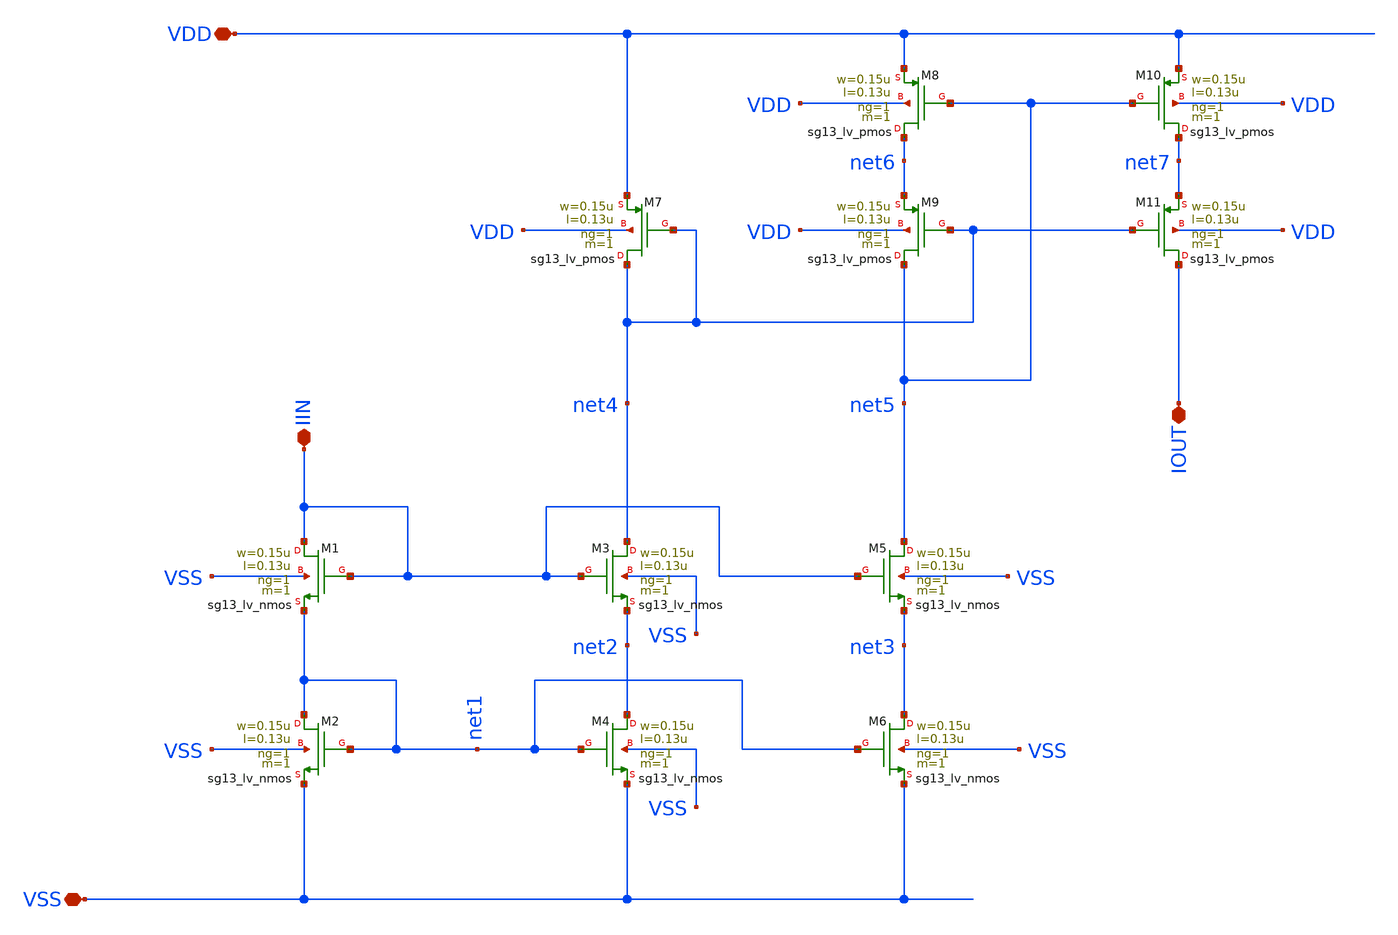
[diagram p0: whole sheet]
** sch_path: analog-db/templates/current_mirror/pmos_current_source/wide_swing_current_mirror_pmos.sch
* Copyright 2026 MacAnalog Research Group
**.subckt wide_swing_current_mirror_pmos VSS IIN VDD IOUT
*.iopin VSS
*.iopin IIN
*.iopin VDD
*.iopin IOUT
XM1 IIN IIN net1 VSS sg13_lv_nmos w=0.15u l=0.13u ng=1 m=1 mm_ok=1
XM2 net1 net1 VSS VSS sg13_lv_nmos w=0.15u l=0.13u ng=1 m=1 mm_ok=1
XM3 net4 IIN net2 VSS sg13_lv_nmos w=0.15u l=0.13u ng=1 m=1 mm_ok=1
XM4 net2 net1 VSS VSS sg13_lv_nmos w=0.15u l=0.13u ng=1 m=1 mm_ok=1
XM5 net5 IIN net3 VSS sg13_lv_nmos w=0.15u l=0.13u ng=1 m=1 mm_ok=1
XM6 net3 net1 VSS VSS sg13_lv_nmos w=0.15u l=0.13u ng=1 m=1 mm_ok=1
XM7 net4 net4 VDD VDD sg13_lv_pmos w=0.15u l=0.13u ng=1 m=1 mm_ok=1
XM8 net6 net5 VDD VDD sg13_lv_pmos w=0.15u l=0.13u ng=1 m=1 mm_ok=1
XM9 net5 net4 net6 VDD sg13_lv_pmos w=0.15u l=0.13u ng=1 m=1 mm_ok=1
XM10 net7 net5 VDD VDD sg13_lv_pmos w=0.15u l=0.13u ng=1 m=1 mm_ok=1
XM11 IOUT net4 net7 VDD sg13_lv_pmos w=0.15u l=0.13u ng=1 m=1 mm_ok=1
**.ends
.end
